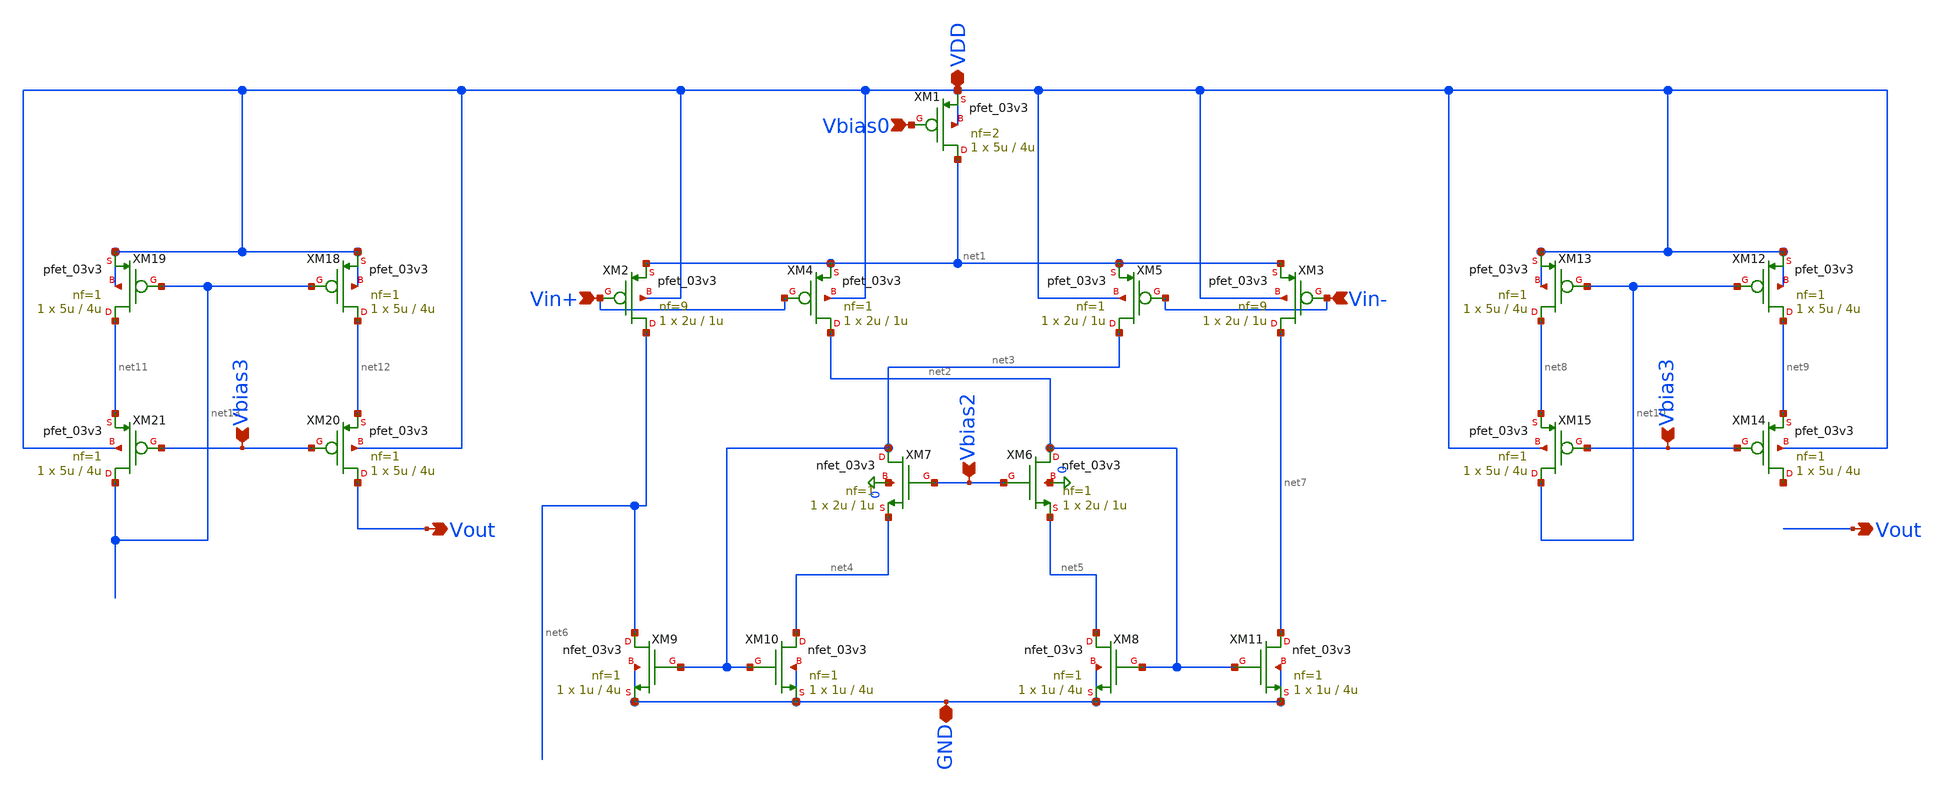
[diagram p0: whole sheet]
** sch_path: analog/B04_diff_OTA.sch
**.subckt B04_diff_OTA VDD Vbias0 Vin+ Vin- Vout Vbias3 Vbias2 GND Vout Vbias3
*.iopin VDD
*.ipin Vbias0
*.ipin Vin+
*.ipin Vin-
*.opin Vout
*.ipin Vbias3
*.ipin Vbias2
*.iopin GND
*.opin Vout
*.ipin Vbias3
XM1 net1 Vbias0 VDD VDD pfet_03v3 L=4u W=5u nf=2 ad='int((nf+1)/2) * W/nf * 0.18u' as='int((nf+2)/2) * W/nf * 0.18u'
+ pd='2*int((nf+1)/2) * (W/nf + 0.18u)' ps='2*int((nf+2)/2) * (W/nf + 0.18u)' nrd='0.18u / W' nrs='0.18u / W'
+ sa=0 sb=0 sd=0 m=1
XM2 net6 Vin+ net1 VDD pfet_03v3 L=1u W=2u nf=9 ad='int((nf+1)/2) * W/nf * 0.18u' as='int((nf+2)/2) * W/nf * 0.18u'
+ pd='2*int((nf+1)/2) * (W/nf + 0.18u)' ps='2*int((nf+2)/2) * (W/nf + 0.18u)' nrd='0.18u / W' nrs='0.18u / W'
+ sa=0 sb=0 sd=0 m=1
XM3 net7 Vin- net1 VDD pfet_03v3 L=1u W=2u nf=9 ad='int((nf+1)/2) * W/nf * 0.18u' as='int((nf+2)/2) * W/nf * 0.18u'
+ pd='2*int((nf+1)/2) * (W/nf + 0.18u)' ps='2*int((nf+2)/2) * (W/nf + 0.18u)' nrd='0.18u / W' nrs='0.18u / W'
+ sa=0 sb=0 sd=0 m=1
XM4 net2 Vin+ net1 VDD pfet_03v3 L=1u W=2u nf=1 ad='int((nf+1)/2) * W/nf * 0.18u' as='int((nf+2)/2) * W/nf * 0.18u'
+ pd='2*int((nf+1)/2) * (W/nf + 0.18u)' ps='2*int((nf+2)/2) * (W/nf + 0.18u)' nrd='0.18u / W' nrs='0.18u / W'
+ sa=0 sb=0 sd=0 m=1
XM5 net3 Vin- net1 VDD pfet_03v3 L=1u W=2u nf=1 ad='int((nf+1)/2) * W/nf * 0.18u' as='int((nf+2)/2) * W/nf * 0.18u'
+ pd='2*int((nf+1)/2) * (W/nf + 0.18u)' ps='2*int((nf+2)/2) * (W/nf + 0.18u)' nrd='0.18u / W' nrs='0.18u / W'
+ sa=0 sb=0 sd=0 m=1
XM6 net2 Vbias2 net5 0 nfet_03v3 L=1u W=2u nf=1 ad='int((nf+1)/2) * W/nf * 0.18u' as='int((nf+2)/2) * W/nf * 0.18u'
+ pd='2*int((nf+1)/2) * (W/nf + 0.18u)' ps='2*int((nf+2)/2) * (W/nf + 0.18u)' nrd='0.18u / W' nrs='0.18u / W'
+ sa=0 sb=0 sd=0 m=1
XM7 net3 Vbias2 net4 0 nfet_03v3 L=1u W=2u nf=1 ad='int((nf+1)/2) * W/nf * 0.18u' as='int((nf+2)/2) * W/nf * 0.18u'
+ pd='2*int((nf+1)/2) * (W/nf + 0.18u)' ps='2*int((nf+2)/2) * (W/nf + 0.18u)' nrd='0.18u / W' nrs='0.18u / W'
+ sa=0 sb=0 sd=0 m=1
XM8 net5 net2 GND GND nfet_03v3 L=4u W=1u nf=1 ad='int((nf+1)/2) * W/nf * 0.18u' as='int((nf+2)/2) * W/nf * 0.18u'
+ pd='2*int((nf+1)/2) * (W/nf + 0.18u)' ps='2*int((nf+2)/2) * (W/nf + 0.18u)' nrd='0.18u / W' nrs='0.18u / W'
+ sa=0 sb=0 sd=0 m=1
XM9 net6 net3 GND GND nfet_03v3 L=4u W=1u nf=1 ad='int((nf+1)/2) * W/nf * 0.18u' as='int((nf+2)/2) * W/nf * 0.18u'
+ pd='2*int((nf+1)/2) * (W/nf + 0.18u)' ps='2*int((nf+2)/2) * (W/nf + 0.18u)' nrd='0.18u / W' nrs='0.18u / W'
+ sa=0 sb=0 sd=0 m=1
XM10 net4 net3 GND GND nfet_03v3 L=4u W=1u nf=1 ad='int((nf+1)/2) * W/nf * 0.18u' as='int((nf+2)/2) * W/nf * 0.18u'
+ pd='2*int((nf+1)/2) * (W/nf + 0.18u)' ps='2*int((nf+2)/2) * (W/nf + 0.18u)' nrd='0.18u / W' nrs='0.18u / W'
+ sa=0 sb=0 sd=0 m=1
XM11 net7 net2 GND GND nfet_03v3 L=4u W=1u nf=1 ad='int((nf+1)/2) * W/nf * 0.18u' as='int((nf+2)/2) * W/nf * 0.18u'
+ pd='2*int((nf+1)/2) * (W/nf + 0.18u)' ps='2*int((nf+2)/2) * (W/nf + 0.18u)' nrd='0.18u / W' nrs='0.18u / W'
+ sa=0 sb=0 sd=0 m=1
XM12 net9 net10 VDD VDD pfet_03v3 L=4u W=5u nf=1 ad='int((nf+1)/2) * W/nf * 0.18u' as='int((nf+2)/2) * W/nf * 0.18u'
+ pd='2*int((nf+1)/2) * (W/nf + 0.18u)' ps='2*int((nf+2)/2) * (W/nf + 0.18u)' nrd='0.18u / W' nrs='0.18u / W'
+ sa=0 sb=0 sd=0 m=1
XM13 net8 net10 VDD VDD pfet_03v3 L=4u W=5u nf=1 ad='int((nf+1)/2) * W/nf * 0.18u' as='int((nf+2)/2) * W/nf * 0.18u'
+ pd='2*int((nf+1)/2) * (W/nf + 0.18u)' ps='2*int((nf+2)/2) * (W/nf + 0.18u)' nrd='0.18u / W' nrs='0.18u / W'
+ sa=0 sb=0 sd=0 m=1
XM14 net14 Vbias3 net9 VDD pfet_03v3 L=4u W=5u nf=1 ad='int((nf+1)/2) * W/nf * 0.18u' as='int((nf+2)/2) * W/nf * 0.18u'
+ pd='2*int((nf+1)/2) * (W/nf + 0.18u)' ps='2*int((nf+2)/2) * (W/nf + 0.18u)' nrd='0.18u / W' nrs='0.18u / W'
+ sa=0 sb=0 sd=0 m=1
XM15 net10 Vbias3 net8 VDD pfet_03v3 L=4u W=5u nf=1 ad='int((nf+1)/2) * W/nf * 0.18u' as='int((nf+2)/2) * W/nf * 0.18u'
+ pd='2*int((nf+1)/2) * (W/nf + 0.18u)' ps='2*int((nf+2)/2) * (W/nf + 0.18u)' nrd='0.18u / W' nrs='0.18u / W'
+ sa=0 sb=0 sd=0 m=1
XM18 net12 net13 VDD VDD pfet_03v3 L=4u W=5u nf=1 ad='int((nf+1)/2) * W/nf * 0.18u' as='int((nf+2)/2) * W/nf * 0.18u'
+ pd='2*int((nf+1)/2) * (W/nf + 0.18u)' ps='2*int((nf+2)/2) * (W/nf + 0.18u)' nrd='0.18u / W' nrs='0.18u / W'
+ sa=0 sb=0 sd=0 m=1
XM19 net11 net13 VDD VDD pfet_03v3 L=4u W=5u nf=1 ad='int((nf+1)/2) * W/nf * 0.18u' as='int((nf+2)/2) * W/nf * 0.18u'
+ pd='2*int((nf+1)/2) * (W/nf + 0.18u)' ps='2*int((nf+2)/2) * (W/nf + 0.18u)' nrd='0.18u / W' nrs='0.18u / W'
+ sa=0 sb=0 sd=0 m=1
XM20 Vout Vbias3 net12 VDD pfet_03v3 L=4u W=5u nf=1 ad='int((nf+1)/2) * W/nf * 0.18u' as='int((nf+2)/2) * W/nf * 0.18u'
+ pd='2*int((nf+1)/2) * (W/nf + 0.18u)' ps='2*int((nf+2)/2) * (W/nf + 0.18u)' nrd='0.18u / W' nrs='0.18u / W'
+ sa=0 sb=0 sd=0 m=1
XM21 net13 Vbias3 net11 VDD pfet_03v3 L=4u W=5u nf=1 ad='int((nf+1)/2) * W/nf * 0.18u' as='int((nf+2)/2) * W/nf * 0.18u'
+ pd='2*int((nf+1)/2) * (W/nf + 0.18u)' ps='2*int((nf+2)/2) * (W/nf + 0.18u)' nrd='0.18u / W' nrs='0.18u / W'
+ sa=0 sb=0 sd=0 m=1
**.ends
.end
